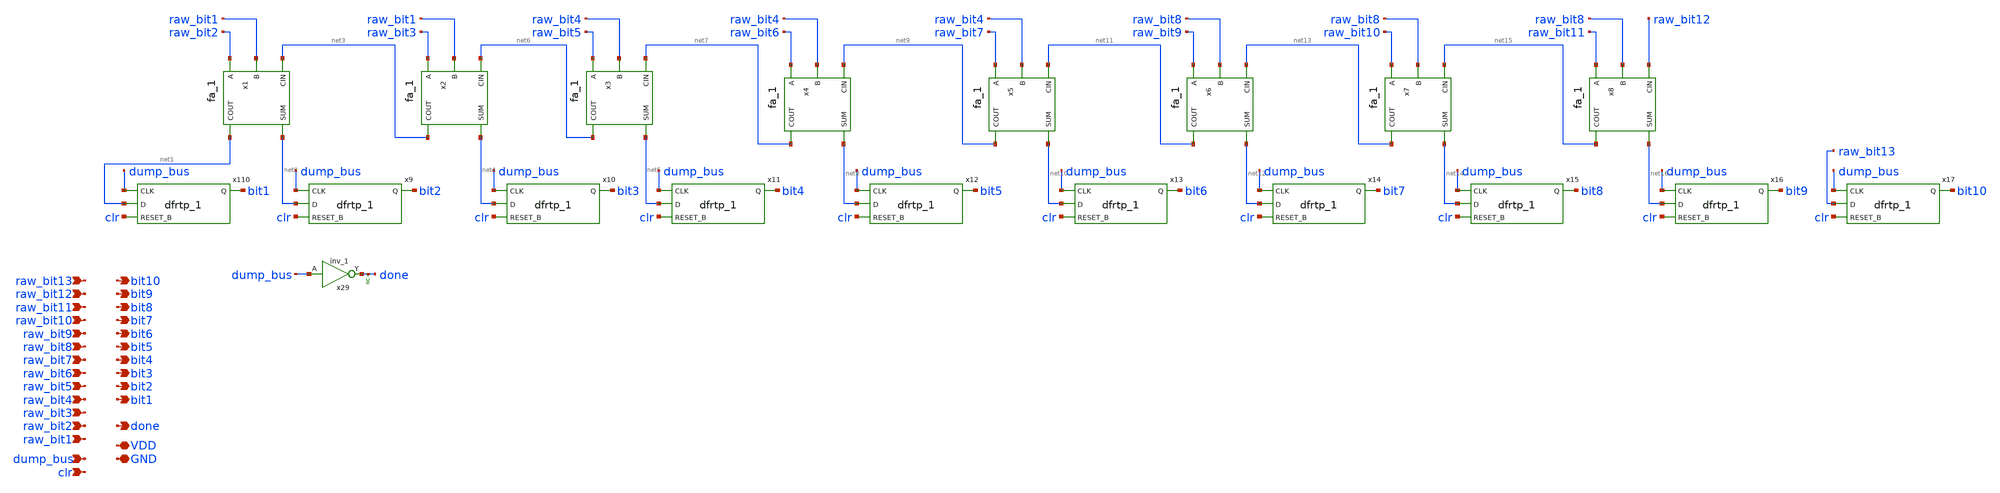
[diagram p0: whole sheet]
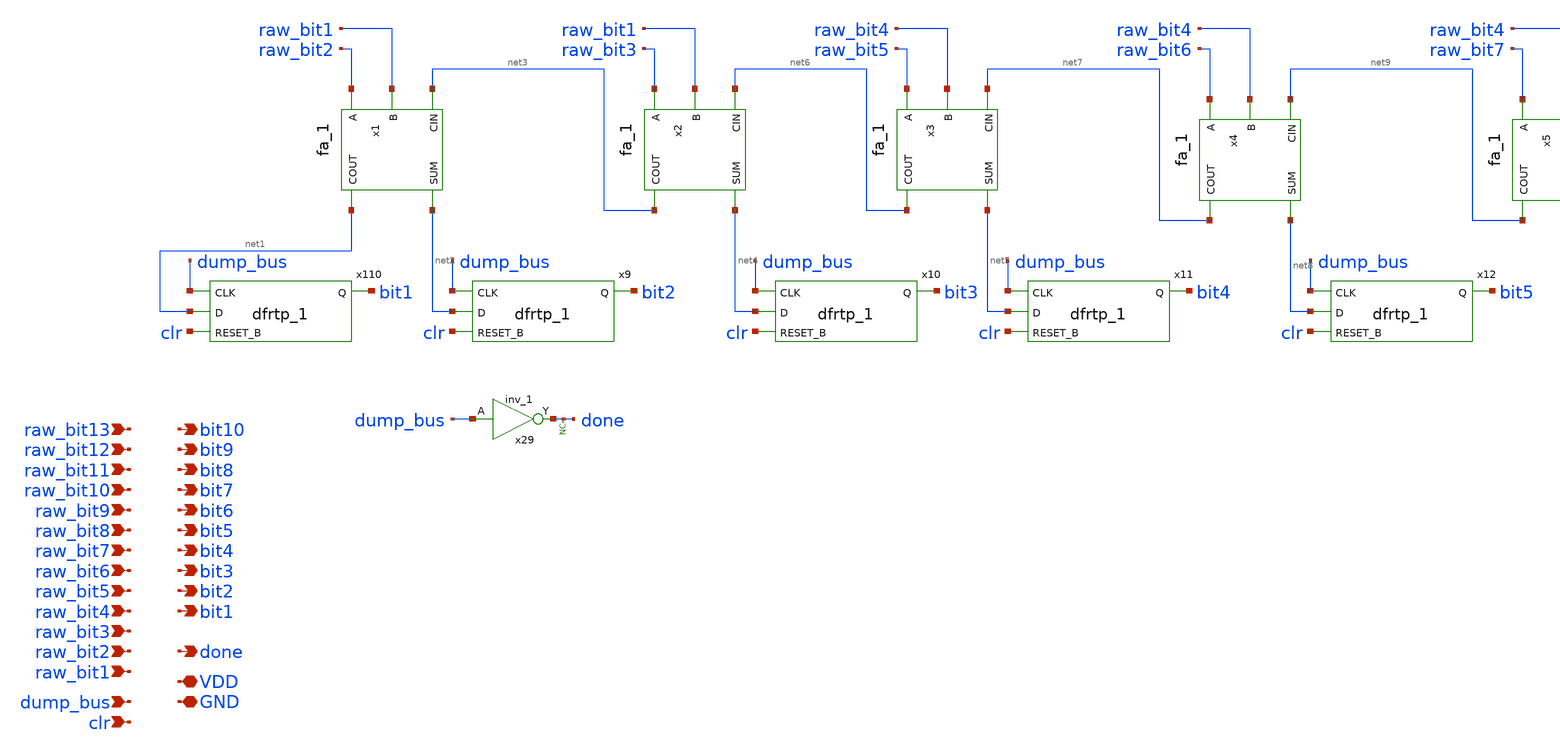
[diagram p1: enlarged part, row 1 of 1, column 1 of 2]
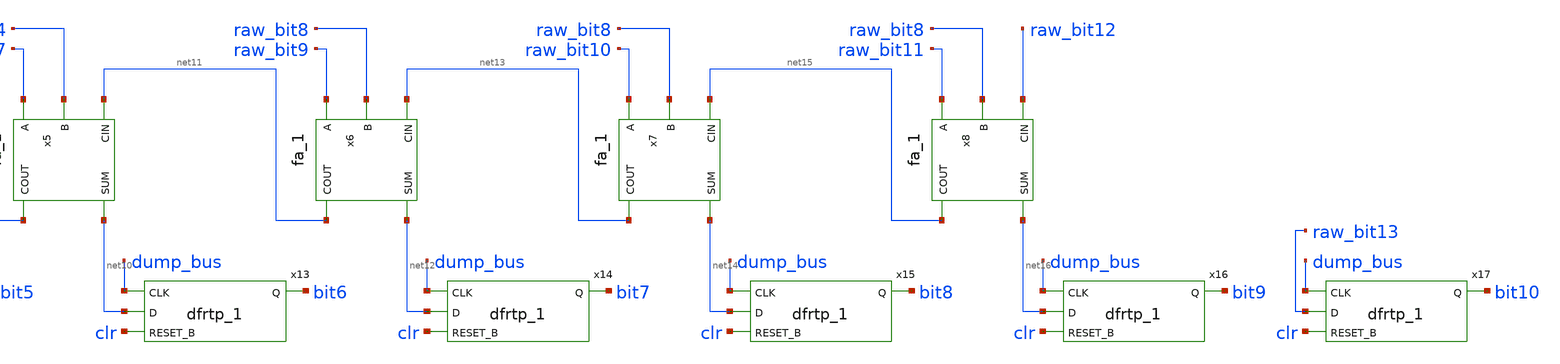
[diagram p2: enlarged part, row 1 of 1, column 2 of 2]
** sch_path: xschem/dec/dec.sch
**.subckt dec raw_bit13 dump_bus clr VDD GND bit10 done bit9 bit8 bit7 bit6 bit5 bit4 bit3 bit2 bit1
*+ raw_bit12 raw_bit11 raw_bit10 raw_bit9 raw_bit8 raw_bit7 raw_bit6 raw_bit5 raw_bit4 raw_bit3 raw_bit2
*+ raw_bit1
*.ipin raw_bit13
*.ipin dump_bus
*.ipin clr
*.iopin VDD
*.iopin GND
*.opin bit10
*.opin done
*.opin bit9
*.opin bit8
*.opin bit7
*.opin bit6
*.opin bit5
*.opin bit4
*.opin bit3
*.opin bit2
*.opin bit1
*.ipin raw_bit12
*.ipin raw_bit11
*.ipin raw_bit10
*.ipin raw_bit9
*.ipin raw_bit8
*.ipin raw_bit7
*.ipin raw_bit6
*.ipin raw_bit5
*.ipin raw_bit4
*.ipin raw_bit3
*.ipin raw_bit2
*.ipin raw_bit1
x1 raw_bit2 raw_bit1 net3 GND GND VDD VDD net1 net2 sky130_fd_sc_hd__fa_1
x110 dump_bus net1 clr GND GND VDD VDD bit1 sky130_fd_sc_hd__dfrtp_1
x2 raw_bit3 raw_bit1 net6 GND GND VDD VDD net3 net4 sky130_fd_sc_hd__fa_1
x3 raw_bit5 raw_bit4 net7 GND GND VDD VDD net6 net5 sky130_fd_sc_hd__fa_1
x4 raw_bit6 raw_bit4 net9 GND GND VDD VDD net7 net8 sky130_fd_sc_hd__fa_1
x5 raw_bit7 raw_bit4 net11 GND GND VDD VDD net9 net10 sky130_fd_sc_hd__fa_1
x6 raw_bit9 raw_bit8 net13 GND GND VDD VDD net11 net12 sky130_fd_sc_hd__fa_1
x7 raw_bit10 raw_bit8 net15 GND GND VDD VDD net13 net14 sky130_fd_sc_hd__fa_1
x8 raw_bit11 raw_bit8 raw_bit12 GND GND VDD VDD net15 net16 sky130_fd_sc_hd__fa_1
x9 dump_bus net2 clr GND GND VDD VDD bit2 sky130_fd_sc_hd__dfrtp_1
x10 dump_bus net4 clr GND GND VDD VDD bit3 sky130_fd_sc_hd__dfrtp_1
x11 dump_bus net5 clr GND GND VDD VDD bit4 sky130_fd_sc_hd__dfrtp_1
x12 dump_bus net8 clr GND GND VDD VDD bit5 sky130_fd_sc_hd__dfrtp_1
x13 dump_bus net10 clr GND GND VDD VDD bit6 sky130_fd_sc_hd__dfrtp_1
x14 dump_bus net12 clr GND GND VDD VDD bit7 sky130_fd_sc_hd__dfrtp_1
x15 dump_bus net14 clr GND GND VDD VDD bit8 sky130_fd_sc_hd__dfrtp_1
x16 dump_bus net16 clr GND GND VDD VDD bit9 sky130_fd_sc_hd__dfrtp_1
x17 dump_bus raw_bit13 clr GND GND VDD VDD bit10 sky130_fd_sc_hd__dfrtp_1
x29 dump_bus GND GND VDD VDD done sky130_fd_sc_hd__inv_1
* noconn done
**.ends
.end
